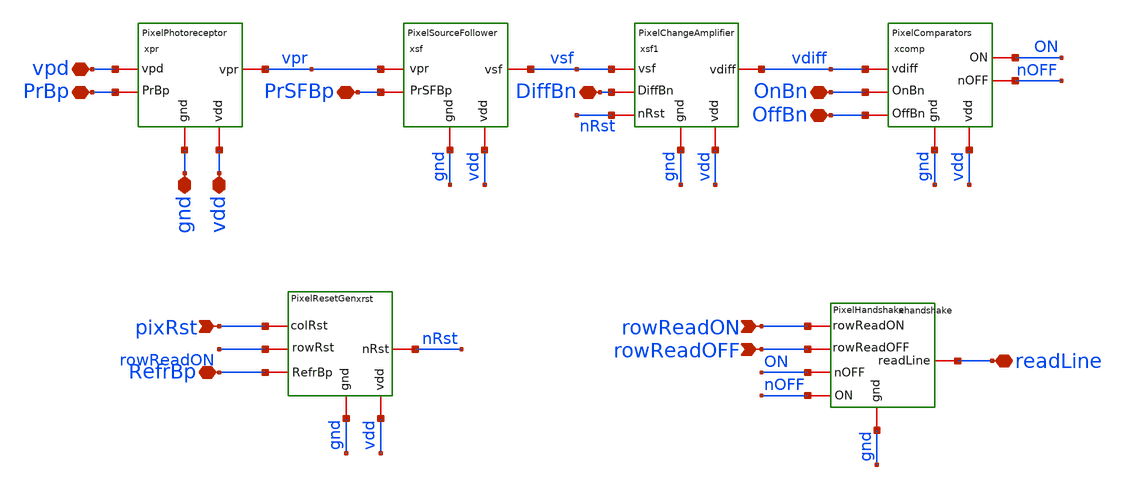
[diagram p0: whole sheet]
** sch_path: analog/xschem/openDVS_pixel.sch
**.subckt openDVS_pixel vpd PrBp gnd vdd PrSFBp DiffBn OnBn OffBn RefrBp pixRst rowReadON rowReadOFF
*+ readLine
*.iopin vpd
*.iopin PrBp
*.iopin gnd
*.iopin vdd
*.iopin PrSFBp
*.iopin DiffBn
*.iopin OnBn
*.iopin OffBn
*.iopin RefrBp
*.ipin pixRst
*.ipin rowReadON
*.ipin rowReadOFF
*.iopin readLine
xpr vdd PrBp gnd vpd vpr PixelPhotoreceptor
xsf vdd PrSFBp gnd vpr vsf PixelSourceFollower
xsf1 vdd DiffBn gnd vsf vdiff nRst PixelChangeAmplifier
xcomp vdd OnBn gnd vdiff ON OffBn nOFF PixelComparators
xhandshake rowReadOFF gnd rowReadON readLine nOFF ON PixelHandshake
xrst rowReadON gnd pixRst nRst RefrBp vdd PixelResetGen
**.ends

* expanding   symbol:  PixelPhotoreceptor.sym # of pins=5
** sym_path: analog/xschem/PixelPhotoreceptor.sym
** sch_path: analog/xschem/PixelPhotoreceptor.sch
.subckt PixelPhotoreceptor vdd PrBp gnd vpd vpr
*.iopin PrBp
*.iopin vdd
*.iopin vpd
*.iopin gnd
*.iopin vpr
XMpd vdd vpr vpd gnd sky130_fd_pr__nfet_01v8 L=0.3 W=0.5 nf=1 ad='int((1 + 1)/2) * 0.5 / 1 * 0.29' as='int((1 + 2)/2) * 0.5 / 1 * 0.29'
+ pd='2*int((1 + 1)/2) * (0.5 / 1 + 0.29)' ps='2*int((1 + 2)/2) * (0.5 / 1 + 0.29)' nrd='0.29 / 0.5 ' nrs='0.29 / 0.5 '
+ sa=0 sb=0 sd=0 mult=1 m=1
XMpr_amp vpr vpd gnd gnd sky130_fd_pr__nfet_01v8 L=0.3 W=0.5 nf=1 ad='int((1 + 1)/2) * 0.5 / 1 * 0.29'
+ as='int((1 + 2)/2) * 0.5 / 1 * 0.29' pd='2*int((1 + 1)/2) * (0.5 / 1 + 0.29)' ps='2*int((1 + 2)/2) * (0.5 / 1 + 0.29)'
+ nrd='0.29 / 0.5 ' nrs='0.29 / 0.5 ' sa=0 sb=0 sd=0 mult=1 m=1
XMprBias vpr PrBp vdd vdd sky130_fd_pr__pfet_01v8_hvt L=0.3 W=1 nf=1 ad='int((1 + 1)/2) * 1 / 1 * 0.29'
+ as='int((1 + 2)/2) * 1 / 1 * 0.29' pd='2*int((1 + 1)/2) * (1 / 1 + 0.29)' ps='2*int((1 + 2)/2) * (1 / 1 + 0.29)'
+ nrd='0.29 / 1 ' nrs='0.29 / 1 ' sa=0 sb=0 sd=0 mult=1 m=1
.ends


* expanding   symbol:  PixelSourceFollower.sym # of pins=5
** sym_path: analog/xschem/PixelSourceFollower.sym
** sch_path: analog/xschem/PixelSourceFollower.sch
.subckt PixelSourceFollower vdd PrSFBp gnd vpr vsf
*.iopin gnd
*.iopin PrSFBp
*.iopin vpr
*.iopin vsf
*.iopin vdd
XMsfBias vsf PrSFBp vdd vdd sky130_fd_pr__pfet_01v8 L=4 W=1 nf=1 ad='int((1 + 1)/2) * 1 / 1 * 0.29' as='int((1 + 2)/2) * 1 / 1 * 0.29'
+ pd='2*int((1 + 1)/2) * (1 / 1 + 0.29)' ps='2*int((1 + 2)/2) * (1 / 1 + 0.29)' nrd='0.29 / 1 ' nrs='0.29 / 1 '
+ sa=0 sb=0 sd=0 mult=1 m=1
XMsf1 gnd vpr vsf vdd sky130_fd_pr__pfet_01v8 L=1 W=2 nf=1 ad='int((1 + 1)/2) * 2 / 1 * 0.29' as='int((1 + 2)/2) * 2 / 1 * 0.29'
+ pd='2*int((1 + 1)/2) * (2 / 1 + 0.29)' ps='2*int((1 + 2)/2) * (2 / 1 + 0.29)' nrd='0.29 / 2 ' nrs='0.29 / 2 '
+ sa=0 sb=0 sd=0 mult=1 m=1
.ends


* expanding   symbol:  PixelChangeAmplifier.sym # of pins=6
** sym_path: analog/xschem/PixelChangeAmplifier.sym
** sch_path: analog/xschem/PixelChangeAmplifier.sch
.subckt PixelChangeAmplifier vdd DiffBn gnd vsf vdiff nRst
*.iopin DiffBn
*.iopin vsf
*.iopin vdd
*.iopin gnd
*.iopin vdiff
*.iopin nRst
XC1 vsf vd sky130_fd_pr__cap_mim_m3_1 W=1 L=1 MF=40 m=40
XC2 vd vdiff sky130_fd_pr__cap_mim_m3_1 W=1 L=1 MF=2 m=2
XMchAmpBias vdiff DiffBn gnd gnd sky130_fd_pr__nfet_01v8 L=2 W=2 nf=1 ad='int((1 + 1)/2) * 2 / 1 * 0.29'
+ as='int((1 + 2)/2) * 2 / 1 * 0.29' pd='2*int((1 + 1)/2) * (2 / 1 + 0.29)' ps='2*int((1 + 2)/2) * (2 / 1 + 0.29)'
+ nrd='0.29 / 2 ' nrs='0.29 / 2 ' sa=0 sb=0 sd=0 mult=1 m=1
XMrst vdiff nRst vd vdd sky130_fd_pr__pfet_01v8_hvt L=0.3 W=1 nf=1 ad='int((1 + 1)/2) * 1 / 1 * 0.29'
+ as='int((1 + 2)/2) * 1 / 1 * 0.29' pd='2*int((1 + 1)/2) * (1 / 1 + 0.29)' ps='2*int((1 + 2)/2) * (1 / 1 + 0.29)'
+ nrd='0.29 / 1 ' nrs='0.29 / 1 ' sa=0 sb=0 sd=0 mult=1 m=1
XMchAmp vdiff vd vdd vdd sky130_fd_pr__pfet_01v8_hvt L=2 W=2 nf=1 ad='int((1 + 1)/2) * 2 / 1 * 0.29'
+ as='int((1 + 2)/2) * 2 / 1 * 0.29' pd='2*int((1 + 1)/2) * (2 / 1 + 0.29)' ps='2*int((1 + 2)/2) * (2 / 1 + 0.29)'
+ nrd='0.29 / 2 ' nrs='0.29 / 2 ' sa=0 sb=0 sd=0 mult=1 m=1
.ends


* expanding   symbol:  PixelComparators.sym # of pins=7
** sym_path: analog/xschem/PixelComparators.sym
** sch_path: analog/xschem/PixelComparators.sch
.subckt PixelComparators vdd OnBn gnd vdiff ON OffBn nOFF
*.iopin OnBn
*.iopin OffBn
*.iopin vdd
*.iopin vdiff
*.iopin gnd
*.iopin ON
*.iopin nOFF
XMonBias ON OnBn gnd gnd sky130_fd_pr__nfet_01v8 L=2 W=2 nf=1 ad='int((1 + 1)/2) * 2 / 1 * 0.29' as='int((1 + 2)/2) * 2 / 1 * 0.29'
+ pd='2*int((1 + 1)/2) * (2 / 1 + 0.29)' ps='2*int((1 + 2)/2) * (2 / 1 + 0.29)' nrd='0.29 / 2 ' nrs='0.29 / 2 '
+ sa=0 sb=0 sd=0 mult=1 m=1
XMoffBias nOFF OffBn gnd gnd sky130_fd_pr__nfet_01v8 L=2 W=2 nf=1 ad='int((1 + 1)/2) * 2 / 1 * 0.29'
+ as='int((1 + 2)/2) * 2 / 1 * 0.29' pd='2*int((1 + 1)/2) * (2 / 1 + 0.29)' ps='2*int((1 + 2)/2) * (2 / 1 + 0.29)'
+ nrd='0.29 / 2 ' nrs='0.29 / 2 ' sa=0 sb=0 sd=0 mult=1 m=1
XMon ON vdiff vdd vdd sky130_fd_pr__pfet_01v8_hvt L=2 W=2 nf=1 ad='int((1 + 1)/2) * 2 / 1 * 0.29' as='int((1 + 2)/2) * 2 / 1 * 0.29'
+ pd='2*int((1 + 1)/2) * (2 / 1 + 0.29)' ps='2*int((1 + 2)/2) * (2 / 1 + 0.29)' nrd='0.29 / 2 ' nrs='0.29 / 2 '
+ sa=0 sb=0 sd=0 mult=1 m=1
XMoff nOFF vdiff vdd vdd sky130_fd_pr__pfet_01v8_hvt L=2 W=2 nf=1 ad='int((1 + 1)/2) * 2 / 1 * 0.29'
+ as='int((1 + 2)/2) * 2 / 1 * 0.29' pd='2*int((1 + 1)/2) * (2 / 1 + 0.29)' ps='2*int((1 + 2)/2) * (2 / 1 + 0.29)'
+ nrd='0.29 / 2 ' nrs='0.29 / 2 ' sa=0 sb=0 sd=0 mult=1 m=1
.ends


* expanding   symbol:  PixelHandshake.sym # of pins=6
** sym_path: analog/xschem/PixelHandshake.sym
** sch_path: analog/xschem/PixelHandshake.sch
.subckt PixelHandshake rowReadOFF gnd rowReadON readLine ON nOFF
*.ipin rowReadON
*.ipin rowReadOFF
*.iopin readLine
*.iopin ON
*.iopin nOFF
*.iopin gnd
XMswON readLine rowReadON readLineONpd gnd sky130_fd_pr__nfet_01v8 L=0.15 W=0.5 nf=1 ad='int((1 + 1)/2) * 0.5 / 1 * 0.29'
+ as='int((1 + 2)/2) * 0.5 / 1 * 0.29' pd='2*int((1 + 1)/2) * (0.5 / 1 + 0.29)' ps='2*int((1 + 2)/2) * (0.5 / 1 + 0.29)'
+ nrd='0.29 / 0.5 ' nrs='0.29 / 0.5 ' sa=0 sb=0 sd=0 mult=1 m=1
XMoutON readLineONpd ON gnd gnd sky130_fd_pr__nfet_01v8 L=0.15 W=0.5 nf=1 ad='int((1 + 1)/2) * 0.5 / 1 * 0.29'
+ as='int((1 + 2)/2) * 0.5 / 1 * 0.29' pd='2*int((1 + 1)/2) * (0.5 / 1 + 0.29)' ps='2*int((1 + 2)/2) * (0.5 / 1 + 0.29)'
+ nrd='0.29 / 0.5 ' nrs='0.29 / 0.5 ' sa=0 sb=0 sd=0 mult=1 m=1
XMswOFF readLine rowReadOFF readLineOFFpd gnd sky130_fd_pr__nfet_01v8 L=0.15 W=0.5 nf=1 ad='int((1 + 1)/2) * 0.5 / 1 * 0.29'
+ as='int((1 + 2)/2) * 0.5 / 1 * 0.29' pd='2*int((1 + 1)/2) * (0.5 / 1 + 0.29)' ps='2*int((1 + 2)/2) * (0.5 / 1 + 0.29)'
+ nrd='0.29 / 0.5 ' nrs='0.29 / 0.5 ' sa=0 sb=0 sd=0 mult=1 m=1
XMoutOFF readLineOFFpd nOFF gnd gnd sky130_fd_pr__nfet_01v8 L=0.15 W=0.5 nf=1 ad='int((1 + 1)/2) * 0.5 / 1 * 0.29'
+ as='int((1 + 2)/2) * 0.5 / 1 * 0.29' pd='2*int((1 + 1)/2) * (0.5 / 1 + 0.29)' ps='2*int((1 + 2)/2) * (0.5 / 1 + 0.29)'
+ nrd='0.29 / 0.5 ' nrs='0.29 / 0.5 ' sa=0 sb=0 sd=0 mult=1 m=1
.ends


* expanding   symbol:  PixelResetGen.sym # of pins=6
** sym_path: analog/xschem/PixelResetGen.sym
** sch_path: analog/xschem/PixelResetGen.sch
.subckt PixelResetGen rowRst gnd colRst nRst RefrBp vdd
*.ipin rowRst
*.ipin colRst
*.iopin RefrBp
*.iopin gnd
*.iopin vdd
*.iopin nRst
XMrefrInv nRst colRst net1 gnd sky130_fd_pr__nfet_01v8 L=0.15 W=0.5 nf=1 ad='int((1 + 1)/2) * 0.5 / 1 * 0.29'
+ as='int((1 + 2)/2) * 0.5 / 1 * 0.29' pd='2*int((1 + 1)/2) * (0.5 / 1 + 0.29)' ps='2*int((1 + 2)/2) * (0.5 / 1 + 0.29)'
+ nrd='0.29 / 0.5 ' nrs='0.29 / 0.5 ' sa=0 sb=0 sd=0 mult=1 m=1
XMrefrBias nRst RefrBp vdd vdd sky130_fd_pr__pfet_01v8 L=8 W=2 nf=1 ad='int((1 + 1)/2) * 2 / 1 * 0.29'
+ as='int((1 + 2)/2) * 2 / 1 * 0.29' pd='2*int((1 + 1)/2) * (2 / 1 + 0.29)' ps='2*int((1 + 2)/2) * (2 / 1 + 0.29)'
+ nrd='0.29 / 2 ' nrs='0.29 / 2 ' sa=0 sb=0 sd=0 mult=1 m=1
XMcapRefr vdd nRst vdd vdd sky130_fd_pr__pfet_01v8_hvt L=8 W=8 nf=1 ad='int((1 + 1)/2) * 8 / 1 * 0.29'
+ as='int((1 + 2)/2) * 8 / 1 * 0.29' pd='2*int((1 + 1)/2) * (8 / 1 + 0.29)' ps='2*int((1 + 2)/2) * (8 / 1 + 0.29)'
+ nrd='0.29 / 8 ' nrs='0.29 / 8 ' sa=0 sb=0 sd=0 mult=1 m=1
XMswON1 net1 rowRst gnd gnd sky130_fd_pr__nfet_01v8 L=0.15 W=0.5 nf=1 ad='int((1 + 1)/2) * 0.5 / 1 * 0.29'
+ as='int((1 + 2)/2) * 0.5 / 1 * 0.29' pd='2*int((1 + 1)/2) * (0.5 / 1 + 0.29)' ps='2*int((1 + 2)/2) * (0.5 / 1 + 0.29)'
+ nrd='0.29 / 0.5 ' nrs='0.29 / 0.5 ' sa=0 sb=0 sd=0 mult=1 m=1
.ends

.end
